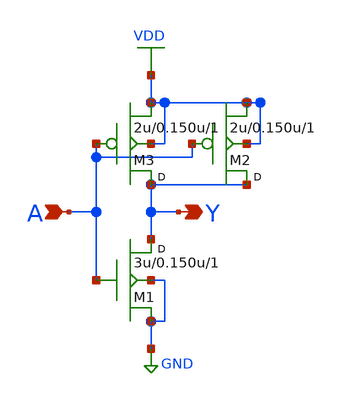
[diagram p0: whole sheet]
** sch_path: lib/xschem/schematics/INVX1.sch
**.subckt INVX1 A Y
*.ipin A
*.opin Y
M3 Y A VDD VDD pmos w=2u l=0.150u m=1
M2 Y A VDD VDD pmos w=2u l=0.150u m=1
M1 Y A GND GND nmos w=3u l=0.150u m=1
**.ends
.GLOBAL GND
.GLOBAL VDD
.end
